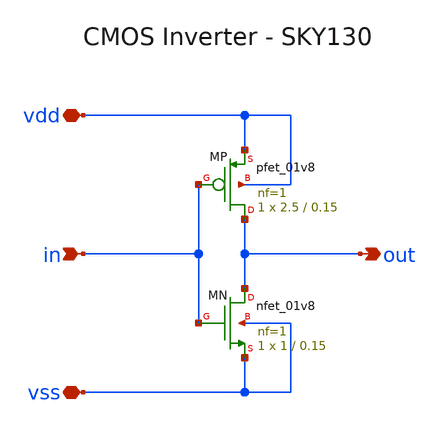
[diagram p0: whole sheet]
** sch_path: lab3/xschem/inv.sch
**.subckt inv in out vdd vss
*.ipin in
*.opin out
*.iopin vdd
*.iopin vss
XMP out in vdd vdd sky130_fd_pr__pfet_01v8 L=0.15 W=2.5 nf=1 ad='int((nf+1)/2) * W/nf * 0.29' as='int((nf+2)/2) * W/nf * 0.29'
+ pd='2*int((nf+1)/2) * (W/nf + 0.29)' ps='2*int((nf+2)/2) * (W/nf + 0.29)' nrd='0.29 / W' nrs='0.29 / W'
+ sa=0 sb=0 sd=0 mult=1 m=1
XMN out in vss vss sky130_fd_pr__nfet_01v8 L=0.15 W=1 nf=1 ad='int((1 + 1)/2) * 1 / 1 * 0.29' as='int((1 + 2)/2) * 1 / 1 * 0.29'
+ pd='2*int((1 + 1)/2) * (1 / 1 + 0.29)' ps='2*int((1 + 2)/2) * (1 / 1 + 0.29)' nrd='0.29 / 1 ' nrs='0.29 / 1 '
+ sa=0 sb=0 sd=0 mult=1 m=1
**.ends
.end
